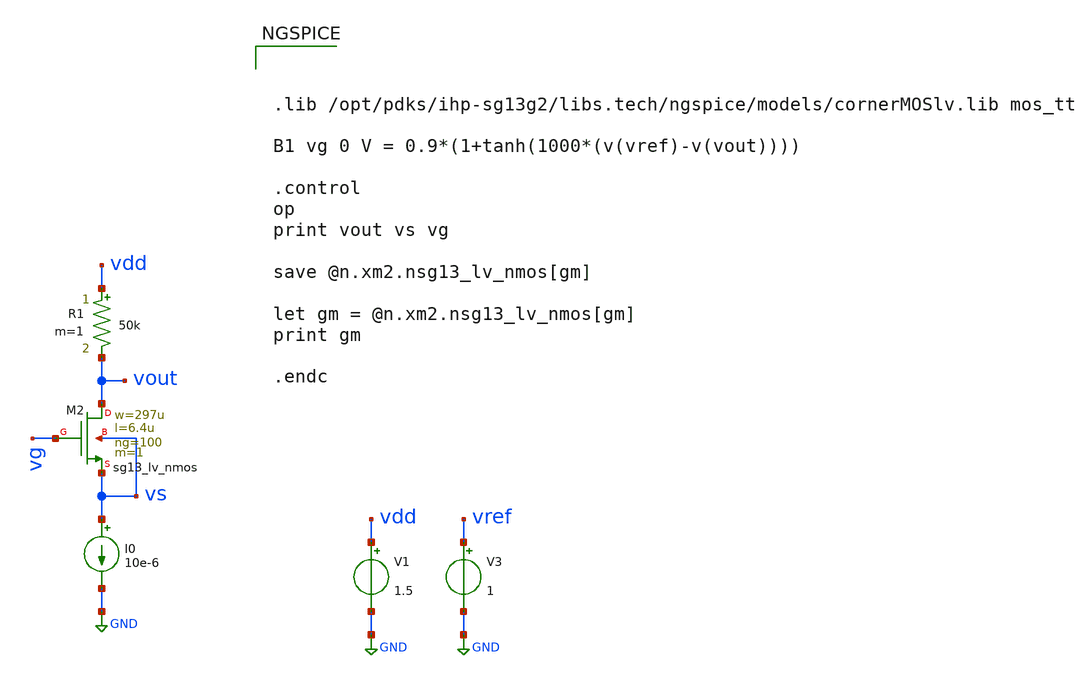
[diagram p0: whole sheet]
** sch_path: test-python/transitor/xschem/nmos.sch
**.subckt nmos
XM2 vout vg vs vs sg13_lv_nmos w=297u l=6.4u ng=100 m=1 mm_ok=1
V1 vdd GND 1.5
V3 vref GND 1
R1 vdd vout 50k m=1
I0 vs GND 10e-6
**** begin user architecture code



.lib /opt/pdks/ihp-sg13g2/libs.tech/ngspice/models/cornerMOSlv.lib mos_tt

B1 vg 0 V = 0.9*(1+tanh(1000*(v(vref)-v(vout))))

.control
op
print vout vs vg

save @n.xm2.nsg13_lv_nmos[gm]

let gm = @n.xm2.nsg13_lv_nmos[gm]
print gm

.endc



**** end user architecture code
**.ends
.GLOBAL GND
.end
